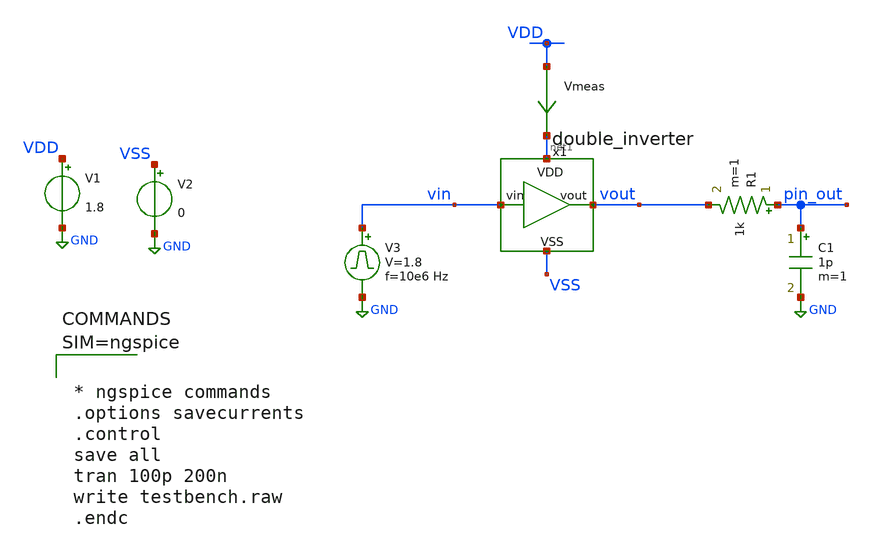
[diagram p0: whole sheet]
** sch_path: xschem/testbench.sch
**.subckt testbench
x1 net1 vin vout VSS double_inverter
V1 VDD GND 1.8
V2 VSS GND 0
R1 pin_out vout 1k m=1
C1 pin_out GND 1p m=1
V3 vin GND pulse 0 1.8 '0.495/ 10e6 ' '0.01/10e6 ' '0.01/10e6 ' '0.49/10e6 ' '1/10e6 '
Vmeas VDD net1 0
.save i(vmeas)
**** begin user architecture code

** opencircuitdesign pdks install
.lib $::SKYWATER_MODELS/sky130.lib.spice tt





* ngspice commands
.options savecurrents
.control
save all
tran 100p 200n
write testbench.raw
.endc



**** end user architecture code
**.ends

* expanding   symbol:  double_inverter.sym # of pins=4
** sym_path: xschem/double_inverter.sym
** sch_path: xschem/double_inverter.sch
.subckt double_inverter VDD vin vout VSS
*.iopin VDD
*.iopin VSS
*.ipin vin
*.opin vout
XM1 net1 vin VSS VSS sky130_fd_pr__nfet_01v8 L=0.15 W=1 nf=1 ad='int((nf+1)/2) * W/nf * 0.29' as='int((nf+2)/2) * W/nf * 0.29'
+ pd='2*int((nf+1)/2) * (W/nf + 0.29)' ps='2*int((nf+2)/2) * (W/nf + 0.29)' nrd='0.29 / W' nrs='0.29 / W'
+ sa=0 sb=0 sd=0 mult=1 m=1
XM2 net1 vin VDD VDD sky130_fd_pr__pfet_01v8 L=0.15 W=1 nf=1 ad='int((nf+1)/2) * W/nf * 0.29' as='int((nf+2)/2) * W/nf * 0.29'
+ pd='2*int((nf+1)/2) * (W/nf + 0.29)' ps='2*int((nf+2)/2) * (W/nf + 0.29)' nrd='0.29 / W' nrs='0.29 / W'
+ sa=0 sb=0 sd=0 mult=1 m=1
XM3 vout net1 VSS VSS sky130_fd_pr__nfet_01v8 L=0.15 W=20 nf=20 ad='int((nf+1)/2) * W/nf * 0.29' as='int((nf+2)/2) * W/nf * 0.29'
+ pd='2*int((nf+1)/2) * (W/nf + 0.29)' ps='2*int((nf+2)/2) * (W/nf + 0.29)' nrd='0.29 / W' nrs='0.29 / W'
+ sa=0 sb=0 sd=0 mult=1 m=1
XM4 vout net1 VDD VDD sky130_fd_pr__pfet_01v8 L=0.15 W=20 nf=20 ad='int((nf+1)/2) * W/nf * 0.29' as='int((nf+2)/2) * W/nf * 0.29'
+ pd='2*int((nf+1)/2) * (W/nf + 0.29)' ps='2*int((nf+2)/2) * (W/nf + 0.29)' nrd='0.29 / W' nrs='0.29 / W'
+ sa=0 sb=0 sd=0 mult=1 m=1
.ends

.GLOBAL GND
.end
